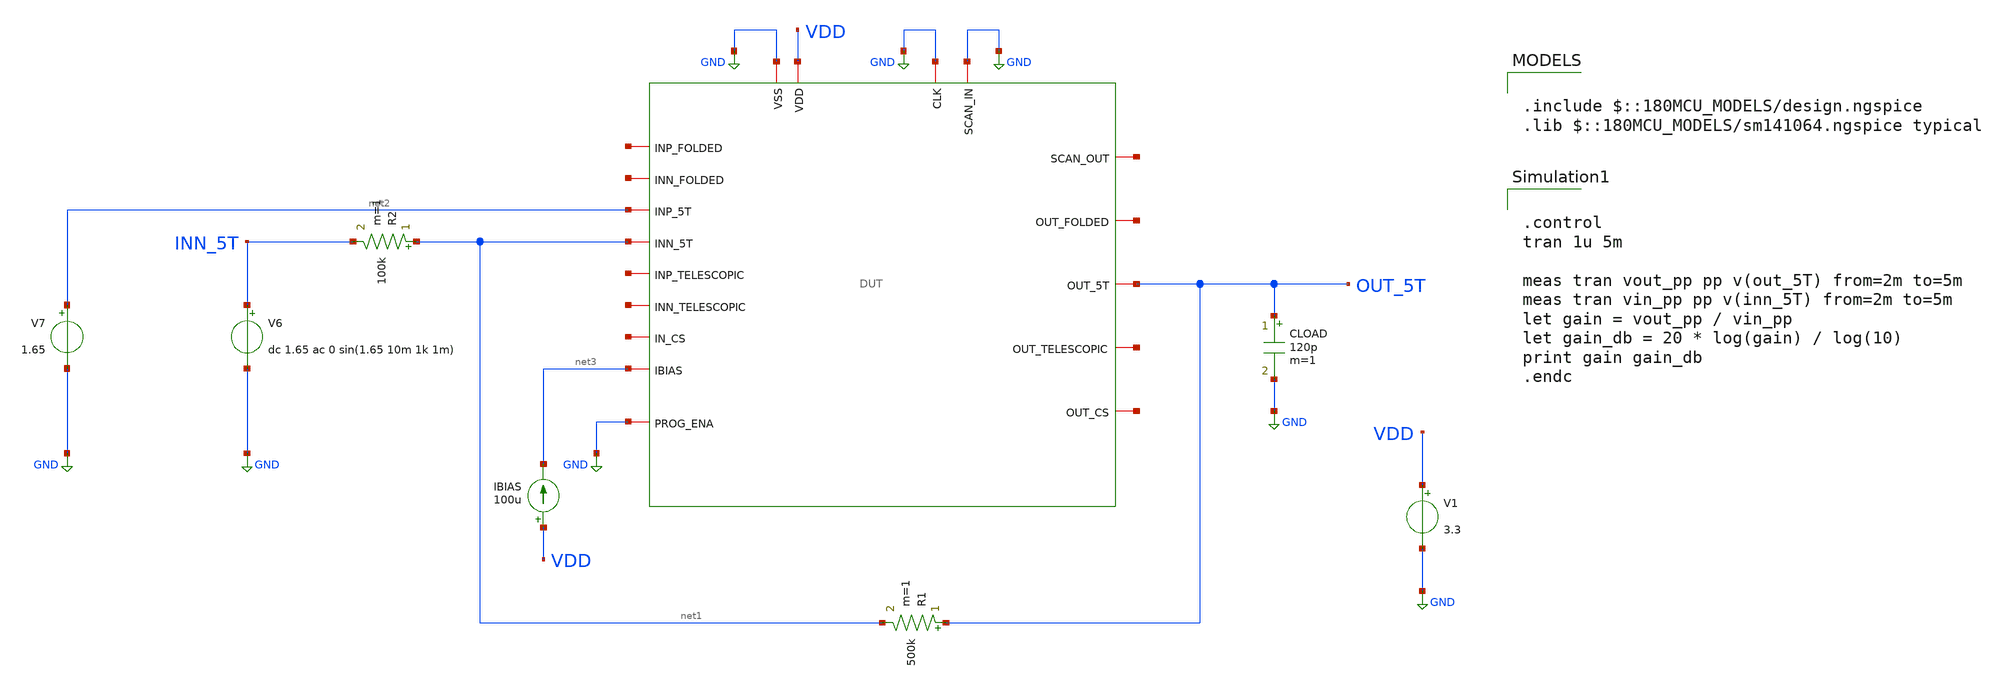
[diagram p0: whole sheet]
** sch_path: designs/libs/verification/ota_5t/defult_sizing/5t_bandwidth_tb.sch
**.subckt 5t_bandwidth_tb
x1 GND net4 GND GND VDD net5 net6 OUT_5T net3 net7 net2 net1 net8 net9 net10 net11 net12 GND DUT
V1 VDD GND 3.3
CLOAD OUT_5T GND 120p m=1
R1 OUT_5T net1 500k m=1
R2 net1 INN_5T 100k m=1
V6 INN_5T GND dc 1.65 ac 0 sin(1.65 10m 1k 1m)
V7 net2 GND 1.65
IBIAS VDD net3 100u
**** begin user architecture code

.include $::180MCU_MODELS/design.ngspice
.lib $::180MCU_MODELS/sm141064.ngspice typical



.control
tran 1u 5m

meas tran vout_pp pp v(out_5T) from=2m to=5m
meas tran vin_pp pp v(inn_5T) from=2m to=5m
let gain = vout_pp / vin_pp
let gain_db = 20 * log(gain) / log(10)
print gain gain_db
.endc


**** end user architecture code
**.ends
.GLOBAL GND
.end
